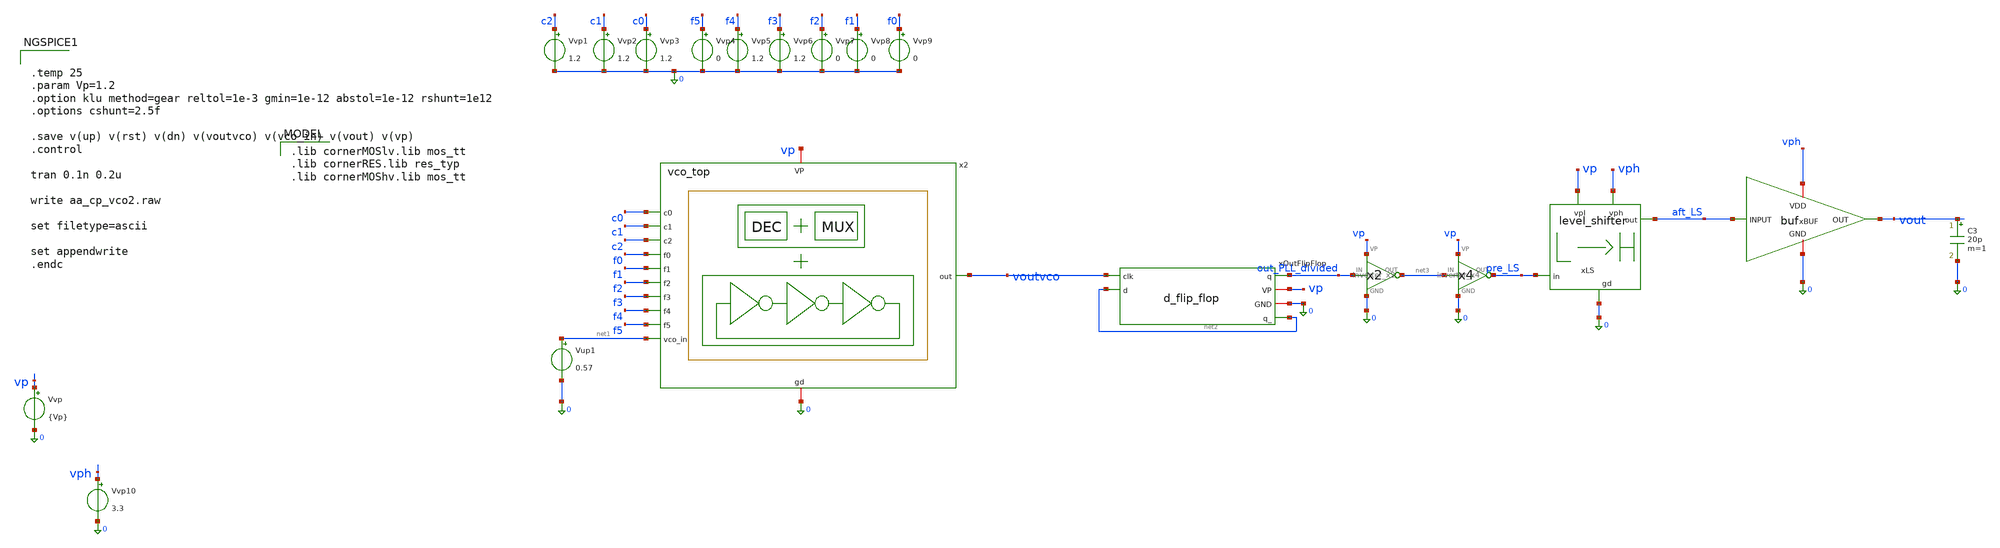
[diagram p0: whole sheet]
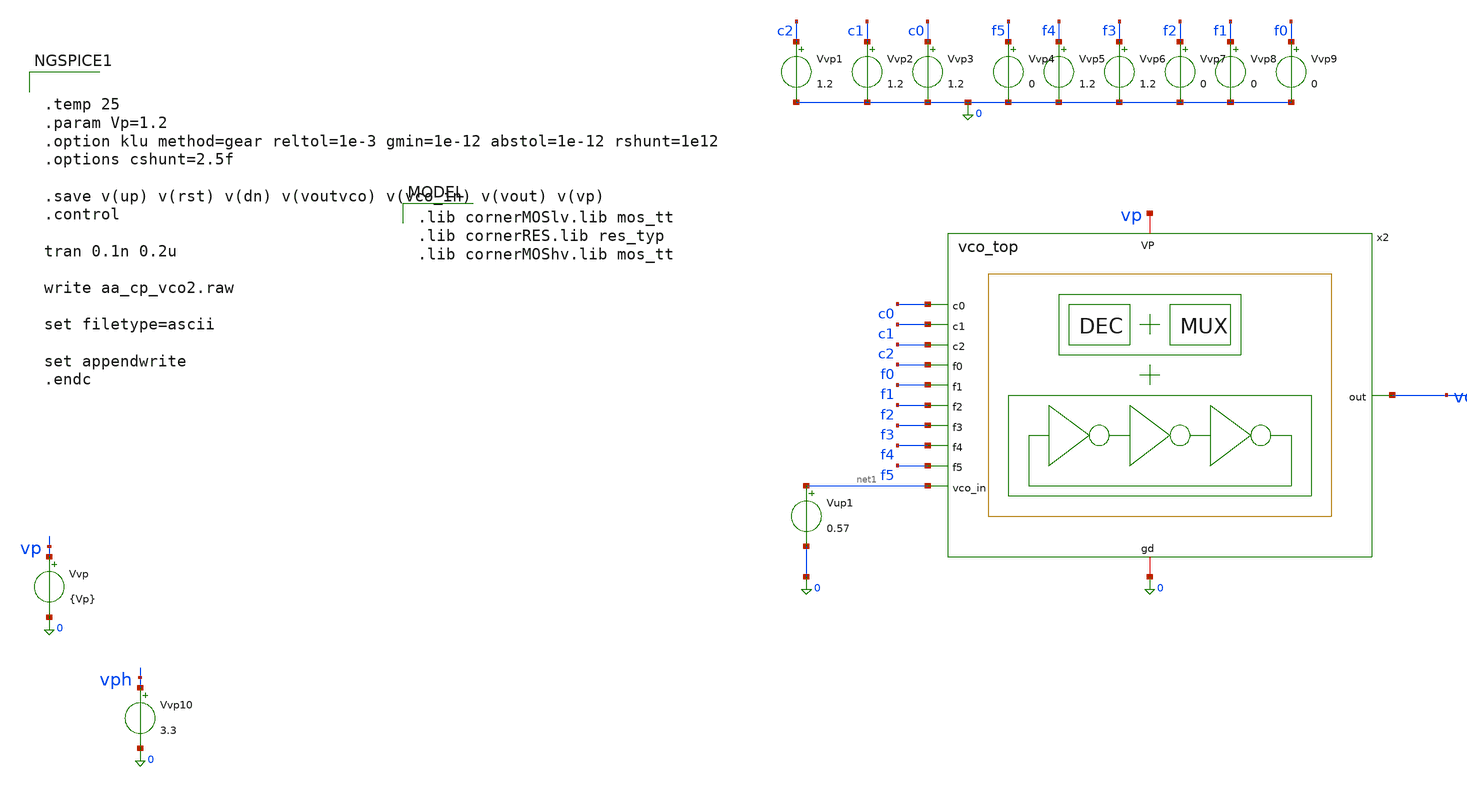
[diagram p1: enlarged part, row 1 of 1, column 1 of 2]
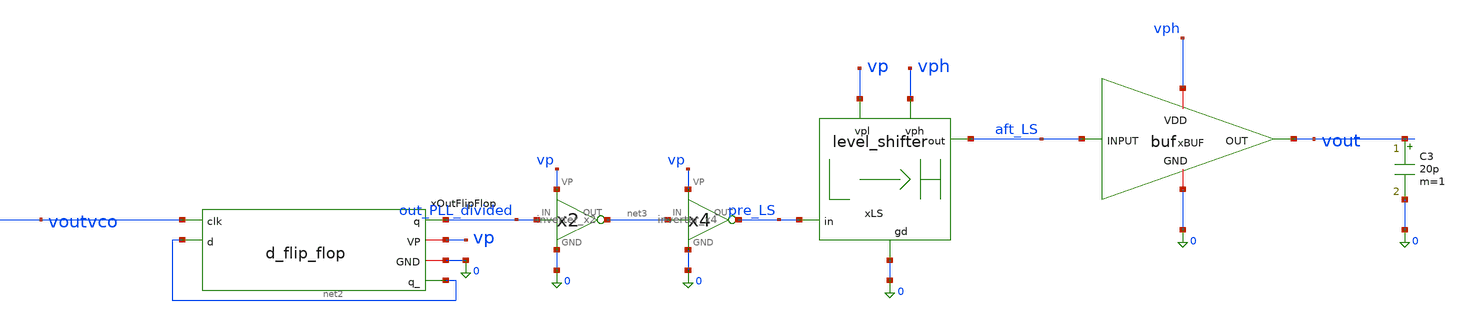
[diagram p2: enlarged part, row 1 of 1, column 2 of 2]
** sch_path: schematics/charge_pump/cp10u_fullvco_tb.sch
**.subckt cp10u_fullvco_tb
Vvp vp 0 {Vp}
Vvp1 c2 0 1.2
Vvp2 c1 0 1.2
Vvp3 c0 0 1.2
Vvp4 f5 0 0
Vvp5 f4 0 1.2
Vvp6 f3 0 1.2
Vvp7 f2 0 0
Vvp8 f1 0 0
Vvp9 f0 0 0
x2 voutvco 0 vp c0 c1 c2 f0 f1 f2 f3 f4 f5 net1 vco_top
xBUF vph aft_LS vout 0 buf
xOutFlipFlop out_PLL_divided vp 0 net2 voutvco net2 d_flip_flop
xLS vph aft_LS vp pre_LS 0 level_shifter
x3 out_PLL_divided net3 vp 0 inverter_x2
x4 net3 pre_LS vp 0 inverter_x4
C3 vout 0 20p m=1
Vup1 net1 0 0.57
Vvp10 vph 0 3.3
**** begin user architecture code
 .lib cornerMOSlv.lib mos_tt
.lib cornerRES.lib res_typ
.lib cornerMOShv.lib mos_tt






.temp 25
.param Vp=1.2
.option klu method=gear reltol=1e-3 gmin=1e-12 abstol=1e-12 rshunt=1e12
.options cshunt=2.5f

.save v(up) v(rst) v(dn) v(voutvco) v(vco_in) v(vout) v(vp)
.control

tran 0.1n 0.2u

write aa_cp_vco2.raw

set filetype=ascii

set appendwrite
.endc


**** end user architecture code
**.ends
.end
